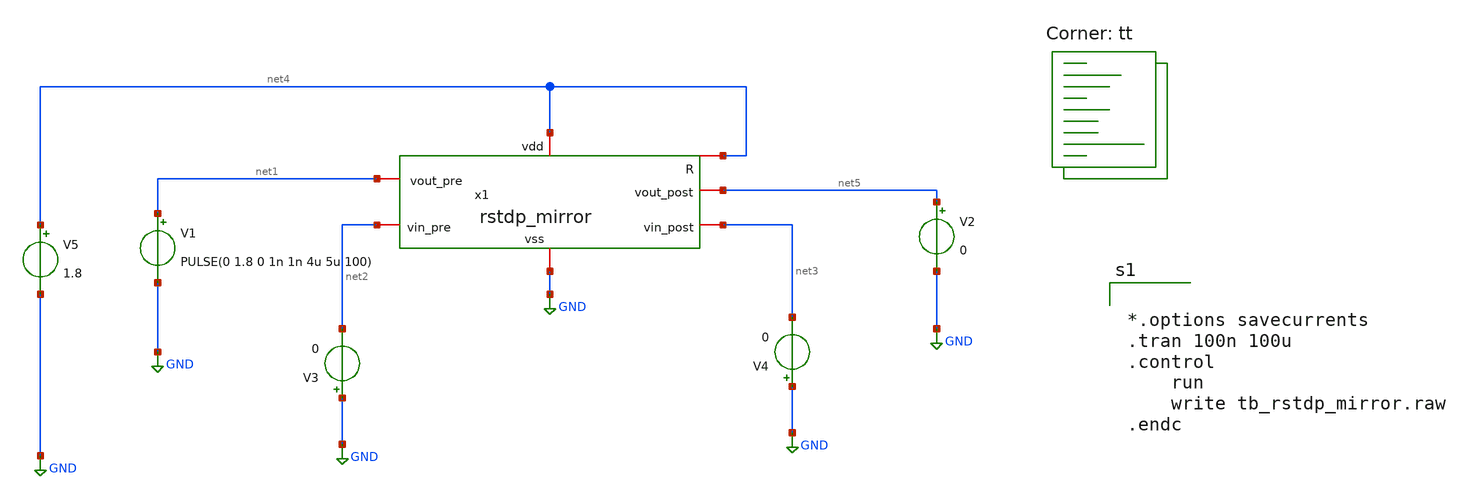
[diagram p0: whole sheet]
** sch_path: Synapse/tb_rstdp_mirror.sch
**.subckt tb_rstdp_mirror
x1 net4 net4 GND net1 net5 net3 net2 rstdp_mirror
V1 net1 GND PULSE(0 1.8 0 1n 1n 4u 5u 100)
V2 net5 GND 0
V3 GND net2 0
V4 GND net3 0
V5 net4 GND 1.8
**** begin user architecture code
.lib $::SKYWATER_MODELS/sky130.lib.spice tt


*.options savecurrents
.tran 100n 100u
.control
	run
	write tb_rstdp_mirror.raw
.endc




** opencircuitdesign pdks install
.inc $::SKYWATER_MODELS/rram_v0.spice

**** end user architecture code
**.ends

* expanding   symbol:  /home/alex/Desktop/EDA/SNN_IPN/Synapse/rstdp_mirror.sym # of pins=7
** sym_path: Synapse/rstdp_mirror.sym
** sch_path: Synapse/rstdp_mirror.sch
.subckt rstdp_mirror vdd R vss vout_pre vout_post vin_post vin_pre
*.iopin vdd
*.iopin vss
*.iopin R
*.iopin vout_post
*.iopin vout_pre
*.iopin vin_post
*.iopin vin_pre
XR2 net1 be rram_v0
XM2 vpre R be vss sky130_fd_pr__nfet_01v8 L=0.15 W=7.5 nf=1 ad='int((nf+1)/2) * W/nf * 0.29' as='int((nf+2)/2) * W/nf * 0.29'
+ pd='2*int((nf+1)/2) * (W/nf + 0.29)' ps='2*int((nf+2)/2) * (W/nf + 0.29)' nrd='0.29 / W' nrs='0.29 / W'
+ sa=0 sb=0 sd=0 mult=1 m=1
XM3 te R vpost vss sky130_fd_pr__nfet_01v8 L=0.15 W=7.5 nf=1 ad='int((nf+1)/2) * W/nf * 0.29' as='int((nf+2)/2) * W/nf * 0.29'
+ pd='2*int((nf+1)/2) * (W/nf + 0.29)' ps='2*int((nf+2)/2) * (W/nf + 0.29)' nrd='0.29 / W' nrs='0.29 / W'
+ sa=0 sb=0 sd=0 mult=1 m=1
XM1 te R vpre vdd sky130_fd_pr__pfet_01v8 L=0.15 W=15 nf=1 ad='int((nf+1)/2) * W/nf * 0.29' as='int((nf+2)/2) * W/nf * 0.29'
+ pd='2*int((nf+1)/2) * (W/nf + 0.29)' ps='2*int((nf+2)/2) * (W/nf + 0.29)' nrd='0.29 / W' nrs='0.29 / W'
+ sa=0 sb=0 sd=0 mult=2 m=2
XM4 vpost R be vdd sky130_fd_pr__pfet_01v8 L=0.15 W=15 nf=1 ad='int((nf+1)/2) * W/nf * 0.29' as='int((nf+2)/2) * W/nf * 0.29'
+ pd='2*int((nf+1)/2) * (W/nf + 0.29)' ps='2*int((nf+2)/2) * (W/nf + 0.29)' nrd='0.29 / W' nrs='0.29 / W'
+ sa=0 sb=0 sd=0 mult=2 m=2
XM7 vpost vout_post vss vss sky130_fd_pr__nfet_01v8 L=0.15 W=1 nf=1 ad='int((1 + 1)/2) * 1 / 1 * 0.29'
+ as='int((1 + 2)/2) * 1 / 1 * 0.29' pd='2*int((1 + 1)/2) * (1 / 1 + 0.29)' ps='2*int((1 + 2)/2) * (1 / 1 + 0.29)'
+ nrd='0.29 / 1 ' nrs='0.29 / 1 ' sa=0 sb=0 sd=0 mult=1 m=1
XM5 vpost vout_post vdd vdd sky130_fd_pr__pfet_01v8 L=0.15 W=2 nf=1 ad='int((nf+1)/2) * W/nf * 0.29'
+ as='int((nf+2)/2) * W/nf * 0.29' pd='2*int((nf+1)/2) * (W/nf + 0.29)' ps='2*int((nf+2)/2) * (W/nf + 0.29)'
+ nrd='0.29 / W' nrs='0.29 / W' sa=0 sb=0 sd=0 mult=1 m=1
XM6 vpre vout_pre vss vss sky130_fd_pr__nfet_01v8 L=0.15 W=1 nf=1 ad='int((1 + 1)/2) * 1 / 1 * 0.29'
+ as='int((1 + 2)/2) * 1 / 1 * 0.29' pd='2*int((1 + 1)/2) * (1 / 1 + 0.29)' ps='2*int((1 + 2)/2) * (1 / 1 + 0.29)'
+ nrd='0.29 / 1 ' nrs='0.29 / 1 ' sa=0 sb=0 sd=0 mult=1 m=1
XM8 vpre vout_pre vdd vdd sky130_fd_pr__pfet_01v8 L=0.15 W=2 nf=1 ad='int((nf+1)/2) * W/nf * 0.29' as='int((nf+2)/2) * W/nf * 0.29'
+ pd='2*int((nf+1)/2) * (W/nf + 0.29)' ps='2*int((nf+2)/2) * (W/nf + 0.29)' nrd='0.29 / W' nrs='0.29 / W'
+ sa=0 sb=0 sd=0 mult=1 m=1
XM9 te te net1 vdd sky130_fd_pr__pfet_01v8 L=0.15 W=2 nf=1 ad='int((nf+1)/2) * W/nf * 0.29' as='int((nf+2)/2) * W/nf * 0.29'
+ pd='2*int((nf+1)/2) * (W/nf + 0.29)' ps='2*int((nf+2)/2) * (W/nf + 0.29)' nrd='0.29 / W' nrs='0.29 / W'
+ sa=0 sb=0 sd=0 mult=1 m=1
XM10 net2 te vdd vdd sky130_fd_pr__pfet_01v8 L=0.15 W=2 nf=1 ad='int((nf+1)/2) * W/nf * 0.29' as='int((nf+2)/2) * W/nf * 0.29'
+ pd='2*int((nf+1)/2) * (W/nf + 0.29)' ps='2*int((nf+2)/2) * (W/nf + 0.29)' nrd='0.29 / W' nrs='0.29 / W'
+ sa=0 sb=0 sd=0 mult=1 m=1
XM12 net1 net1 te vdd sky130_fd_pr__pfet_01v8 L=0.15 W=2 nf=1 ad='int((nf+1)/2) * W/nf * 0.29' as='int((nf+2)/2) * W/nf * 0.29'
+ pd='2*int((nf+1)/2) * (W/nf + 0.29)' ps='2*int((nf+2)/2) * (W/nf + 0.29)' nrd='0.29 / W' nrs='0.29 / W'
+ sa=0 sb=0 sd=0 mult=1 m=1
XM13 net3 net1 vdd vdd sky130_fd_pr__pfet_01v8 L=0.15 W=2 nf=1 ad='int((nf+1)/2) * W/nf * 0.29' as='int((nf+2)/2) * W/nf * 0.29'
+ pd='2*int((nf+1)/2) * (W/nf + 0.29)' ps='2*int((nf+2)/2) * (W/nf + 0.29)' nrd='0.29 / W' nrs='0.29 / W'
+ sa=0 sb=0 sd=0 mult=1 m=1
XM15 net2 net2 vin_post vss sky130_fd_pr__nfet_01v8 L=0.15 W=1 nf=1 ad='int((nf+1)/2) * W/nf * 0.29'
+ as='int((nf+2)/2) * W/nf * 0.29' pd='2*int((nf+1)/2) * (W/nf + 0.29)' ps='2*int((nf+2)/2) * (W/nf + 0.29)'
+ nrd='0.29 / W' nrs='0.29 / W' sa=0 sb=0 sd=0 mult=1 m=1
XM16 net3 net3 vin_pre vss sky130_fd_pr__nfet_01v8 L=0.15 W=1 nf=1 ad='int((nf+1)/2) * W/nf * 0.29' as='int((nf+2)/2) * W/nf * 0.29'
+ pd='2*int((nf+1)/2) * (W/nf + 0.29)' ps='2*int((nf+2)/2) * (W/nf + 0.29)' nrd='0.29 / W' nrs='0.29 / W'
+ sa=0 sb=0 sd=0 mult=1 m=1
.ends

.GLOBAL GND
.end
